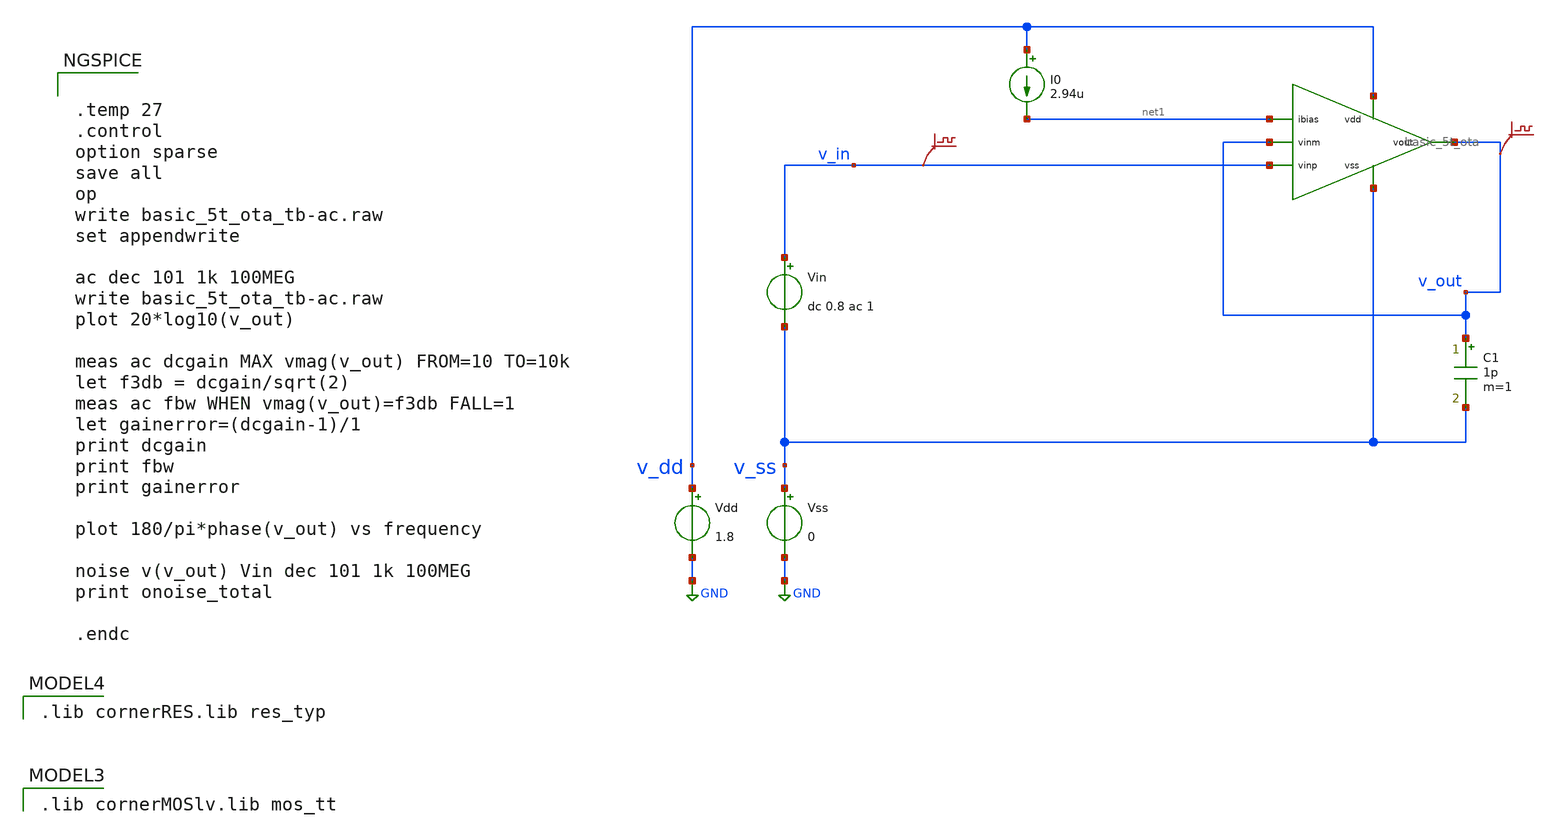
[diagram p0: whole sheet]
** sch_path: design/basic_5t_ota_tb_ac.sch
**.subckt basic_5t_ota_tb_ac
Vdd v_dd GND 1.8
Vss v_ss GND 0
C1 v_out v_ss 1p m=1
Vin v_in v_ss dc 0.8 ac 1
I0 v_dd net1 2.94u
.save v(v_in)
.save v(v_out)
x1 v_dd v_out net1 v_out v_in v_ss basic_5t_ota
**** begin user architecture code


.temp 27
.control
option sparse
save all
op
write basic_5t_ota_tb-ac.raw
set appendwrite

ac dec 101 1k 100MEG
write basic_5t_ota_tb-ac.raw
plot 20*log10(v_out)

meas ac dcgain MAX vmag(v_out) FROM=10 TO=10k
let f3db = dcgain/sqrt(2)
meas ac fbw WHEN vmag(v_out)=f3db FALL=1
let gainerror=(dcgain-1)/1
print dcgain
print fbw
print gainerror

plot 180/pi*phase(v_out) vs frequency

noise v(v_out) Vin dec 101 1k 100MEG
print onoise_total

.endc


 .lib cornerMOSlv.lib mos_tt

 .lib cornerRES.lib res_typ

**** end user architecture code
**.ends
.GLOBAL GND
.end
